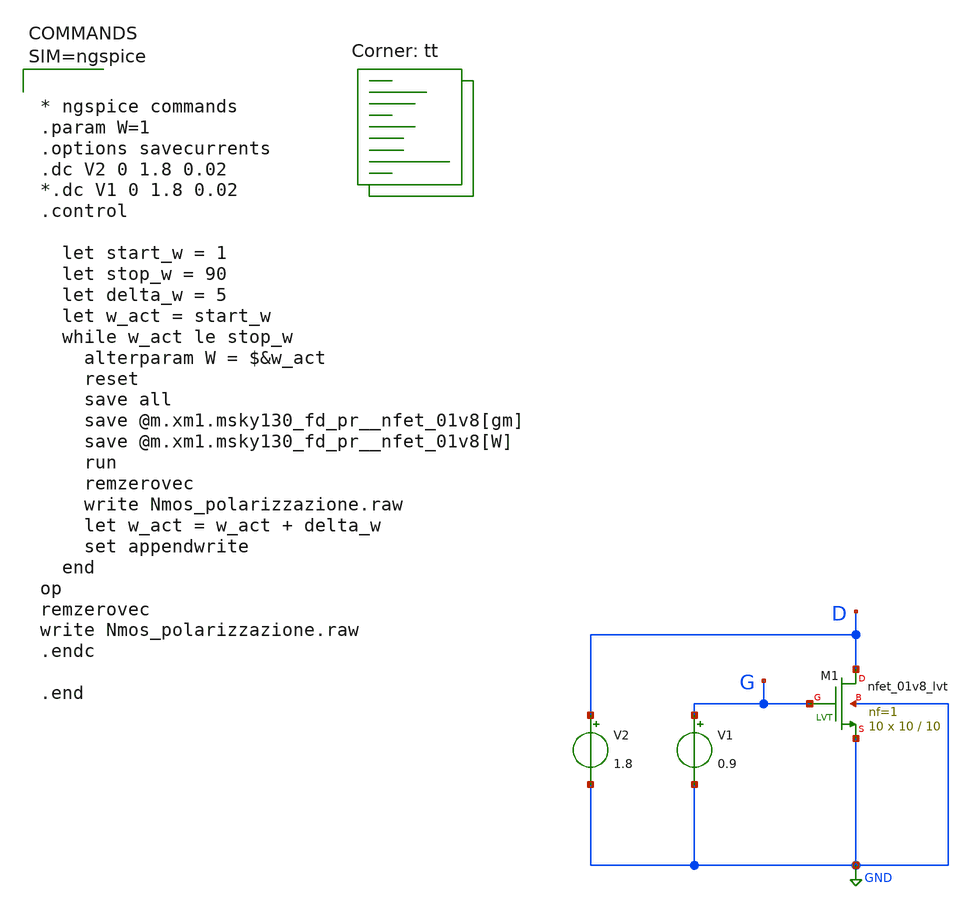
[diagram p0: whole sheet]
** sch_path: xschem/Nmos_polarizzazione.sch
**.subckt Nmos_polarizzazione
V2 D GND 1.8
V1 G GND 0.9
XM1 D G GND GND sky130_fd_pr__nfet_01v8_lvt L=10 W=10 nf=1 ad='int((nf+1)/2) * W/nf * 0.29' as='int((nf+2)/2) * W/nf * 0.29'
+ pd='2*int((nf+1)/2) * (W/nf + 0.29)' ps='2*int((nf+2)/2) * (W/nf + 0.29)' nrd='0.29 / W' nrs='0.29 / W'
+ sa=0 sb=0 sd=0 mult=10 m=10
**** begin user architecture code
.lib $::SKYWATER_MODELS/sky130.lib.spice tt



* ngspice commands
.param W=1
.options savecurrents
.dc V2 0 1.8 0.02
*.dc V1 0 1.8 0.02
.control

  let start_w = 1
  let stop_w = 90
  let delta_w = 5
  let w_act = start_w
  while w_act le stop_w
    alterparam W = $&w_act
    reset
    save all
    save @m.xm1.msky130_fd_pr__nfet_01v8[gm]
    save @m.xm1.msky130_fd_pr__nfet_01v8[W]
    run
    remzerovec
    write Nmos_polarizzazione.raw
    let w_act = w_act + delta_w
    set appendwrite
  end
op
remzerovec
write Nmos_polarizzazione.raw
.endc

.end



**** end user architecture code
**.ends
.GLOBAL GND
.end
